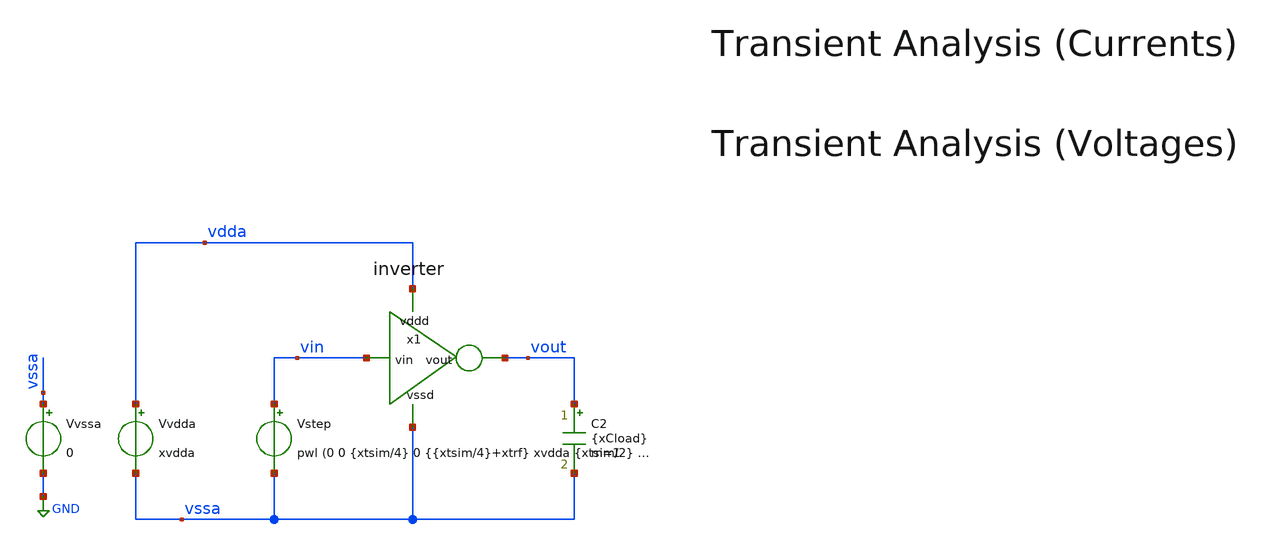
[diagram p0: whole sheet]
** sch_path: Inverter_testcase/inverter_tb.sch
**.subckt inverter_tb
Vvssa vssa GND 0
Vvdda vdda vssa xvdda
Vstep vin vssa pwl (0 0 {xtsim/4} 0 {{xtsim/4}+xtrf} xvdda {xtsim/2} xvdda {{xtsim/2}+xtrf} 0)
C2 vout vssa {xCload} m=1
x1 vin vout vdda vssa inverter
**** begin user architecture code

** opencircuitdesign pdks install
.lib /home/slice/pdk/iHP/IHP-Open-PDK/ihp-sg13g2/libs.tech/ngspice/models/cornerMOSlv.lib mos_tt
*.include /home/slice/xschem/tb_inverter/PEX/RC/output/inverter2__TOP/magic_RC/inverter.spice

* Parameters
.param xvdda = 1.8
.csparam xvdda_var = 'xvdda'
.param xCload = 50f
.param xtrf = 20p
.param xtsim = 5u
.csparam xtsim_var = 'xtsim'

* vlogA instantiation
.model OTA_vcvs OTA_vcvs

  ** must save the below for DCOP analysis to be back annotated onto the schematic
  .option savecurrents
  .save

  +  @n.xinv.xM_NMOS.nsg13_lv_nmos[vgs]
  +  @n.xinv.xM_NMOS.nsg13_lv_nmos[vds]
  +  @n.xinv.xM_NMOS.nsg13_lv_nmos[vth]
  +  @n.xinv.xM_NMOS.nsg13_lv_nmos[gds]
  +  @n.xinv.xM_NMOS.nsg13_lv_nmos[gm]
  +  @n.xinv.xM_NMOS.nsg13_lv_nmos[ids]
  +  @n.xinv.xM_NMOS.nsg13_lv_nmos[vsat]

  +  @n.xinv.xM_PMOS.nsg13_lv_pmos[vgs]
  +  @n.xinv.xM_PMOS.nsg13_lv_pmos[vds]
  +  @n.xinv.xM_PMOS.nsg13_lv_pmos[vth]
  +  @n.xinv.xM_PMOS.nsg13_lv_pmos[gds]
  +  @n.xinv.xM_PMOS.nsg13_lv_pmos[gm]
  +  @n.xinv.xM_PMOS.nsg13_lv_pmos[ids]
  +  @n.xinv.xM_PMOS.nsg13_lv_pmos[vsat]


  .save v(vout) v(vin) v(vdda) v(vssa)
  .save i(xinv.vdda)

  .control
  pre_osdi OTA_vcvs.osdi
  save all

** 1. DCOP ANALYSIS **

  op
 * set filetype=ascii
  remzerovec
  write tb_inv_op.raw

** 2. TRAN ANALYSIS **

  tran 1n $&xtsim_var
  remzerovec
  write tb_inv_tran.raw

** 3. MEASURES **

  echo --
  meas TRAN t_90_10 TRIG v(vout) VAL=0.9*xvdda_var FALL=1 TARG v(vout) VAL=0.1*xvdda_var FALL=1
  meas TRAN t_10_90 TRIG v(vout) VAL=0.1*xvdda_var RISE=1 TARG v(vout) VAL=0.9*xvdda_var RISE=1
  echo --

  setplot
*quit 0
.endc




**** end user architecture code
**.ends

* expanding   symbol:  inverter.sym # of pins=4
** sym_path: tb_inverter_demo/inverter.sym
** sch_path: tb_inverter_demo/inverter.sch
.subckt inverter vin vout vddd vssd
*.ipin vddd
*.ipin vssd
*.ipin vin
*.opin vout
XM_PMOS vout vin vddd vddd sg13_lv_pmos w=0.15u l=0.13u ng=1 m=2 mm_ok=1
XM_NMOS vout vin vssd vssd sg13_lv_nmos w=0.15u l=0.13u ng=1 m=1 mm_ok=1
.ends

.GLOBAL GND
.end
